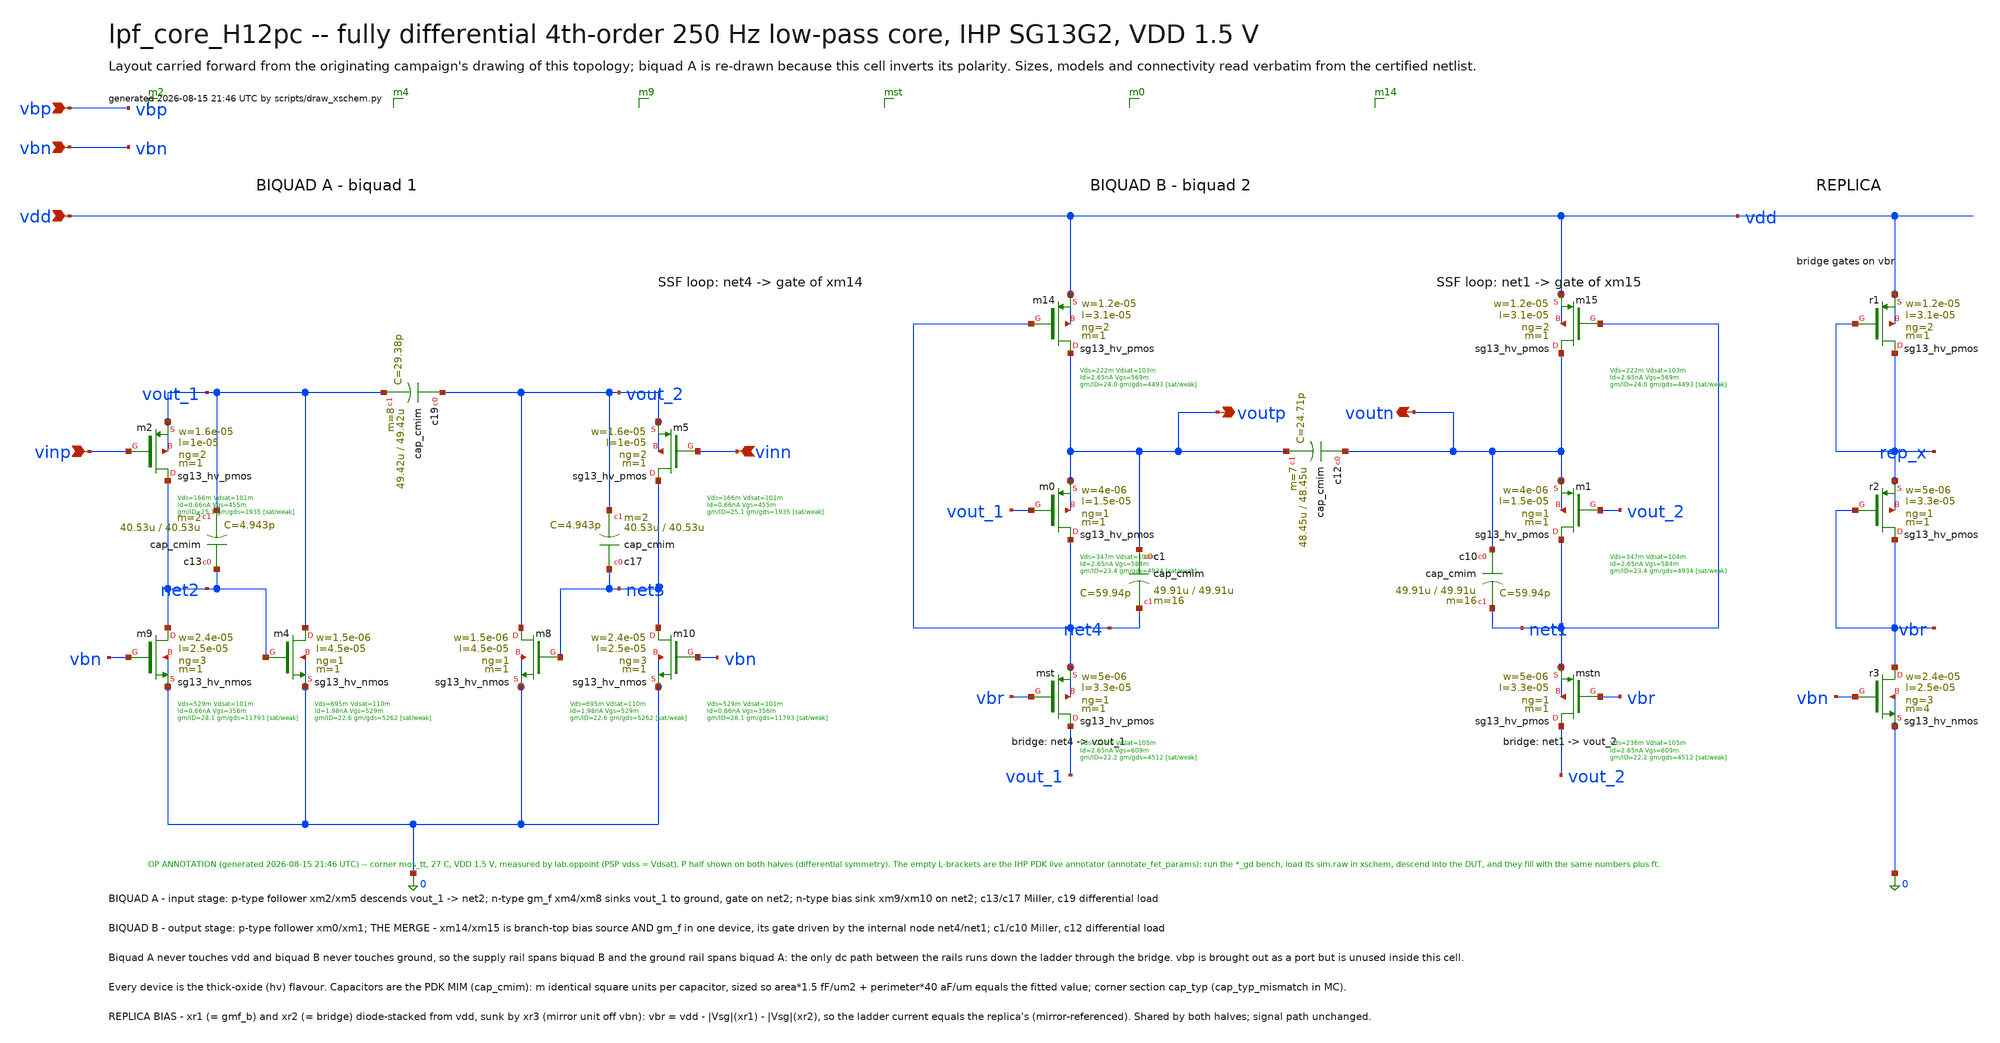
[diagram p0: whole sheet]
** sch_path: signoff/post-pvt/H12-pdk-cap/lpf_core_H12pc.sch
**.subckt lpf_core_H12pc vinp vinn voutp voutn vdd vbn vbp
*.ipin vinp
*.ipin vinn
*.opin voutp
*.opin voutn
*.ipin vdd
*.ipin vbn
*.ipin vbp
Xm2 net2 vinp vout_1 vout_1 sg13_hv_pmos w=1.6e-05 l=1e-05 ng=2 m=1 mm_ok=1
Xm5 net3 vinn vout_2 vout_2 sg13_hv_pmos w=1.6e-05 l=1e-05 ng=2 m=1 mm_ok=1
Xm4 vout_1 net2 0 0 sg13_hv_nmos w=1.5e-06 l=4.5e-05 ng=1 m=1 mm_ok=1
Xm8 vout_2 net3 0 0 sg13_hv_nmos w=1.5e-06 l=4.5e-05 ng=1 m=1 mm_ok=1
Xm9 net2 vbn 0 0 sg13_hv_nmos w=2.4e-05 l=2.5e-05 ng=3 m=1 mm_ok=1
Xm10 net3 vbn 0 0 sg13_hv_nmos w=2.4e-05 l=2.5e-05 ng=3 m=1 mm_ok=1
Xmst vout_1 vbr net4 net4 sg13_hv_pmos w=5e-06 l=3.3e-05 ng=1 m=1 mm_ok=1
Xmstn vout_2 vbr net1 net1 sg13_hv_pmos w=5e-06 l=3.3e-05 ng=1 m=1 mm_ok=1
Xm0 net4 vout_1 voutp voutp sg13_hv_pmos w=4e-06 l=1.5e-05 ng=1 m=1 mm_ok=1
Xm1 net1 vout_2 voutn voutn sg13_hv_pmos w=4e-06 l=1.5e-05 ng=1 m=1 mm_ok=1
Xm14 voutp net4 vdd vdd sg13_hv_pmos w=1.2e-05 l=3.1e-05 ng=2 m=1 mm_ok=1
Xm15 voutn net1 vdd vdd sg13_hv_pmos w=1.2e-05 l=3.1e-05 ng=2 m=1 mm_ok=1
Xr1 rep_x rep_x vdd vdd sg13_hv_pmos w=1.2e-05 l=3.1e-05 ng=2 m=1 mm_ok=1
Xr2 vbr vbr rep_x rep_x sg13_hv_pmos w=5e-06 l=3.3e-05 ng=1 m=1 mm_ok=1
Xr3 vbr vbn 0 0 sg13_hv_nmos w=2.4e-05 l=2.5e-05 ng=3 m=4 mm_ok=1
Xc13 net2 vout_1 cap_cmim w=40.53u l=40.53u m=2 mm_ok=1
Xc17 net3 vout_2 cap_cmim w=40.53u l=40.53u m=2 mm_ok=1
Xc19 vout_2 vout_1 cap_cmim w=49.42u l=49.42u m=8 mm_ok=1
Xc1 voutp net4 cap_cmim w=49.91u l=49.91u m=16 mm_ok=1
Xc10 voutn net1 cap_cmim w=49.91u l=49.91u m=16 mm_ok=1
Xc12 voutn voutp cap_cmim w=48.45u l=48.45u m=7 mm_ok=1
**.ends
.end
